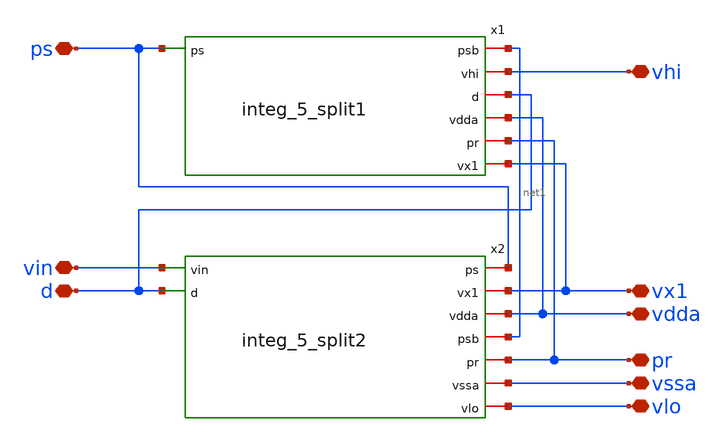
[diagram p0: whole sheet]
** sch_path: 5_Design/4_Layout/Team 5/xschem/integ_5_splitTop1.sch
**.subckt integ_5_splitTop1 d vin ps vhi vx1 vdda pr vssa vlo
*.iopin d
*.iopin vin
*.iopin ps
*.iopin vhi
*.iopin vx1
*.iopin vdda
*.iopin pr
*.iopin vssa
*.iopin vlo
x1 ps net1 vhi d vdda pr vx1 integ_5_split1
x2 ps vin vx1 d vdda net1 pr vssa vlo integ_5_split2
**.ends
.end
